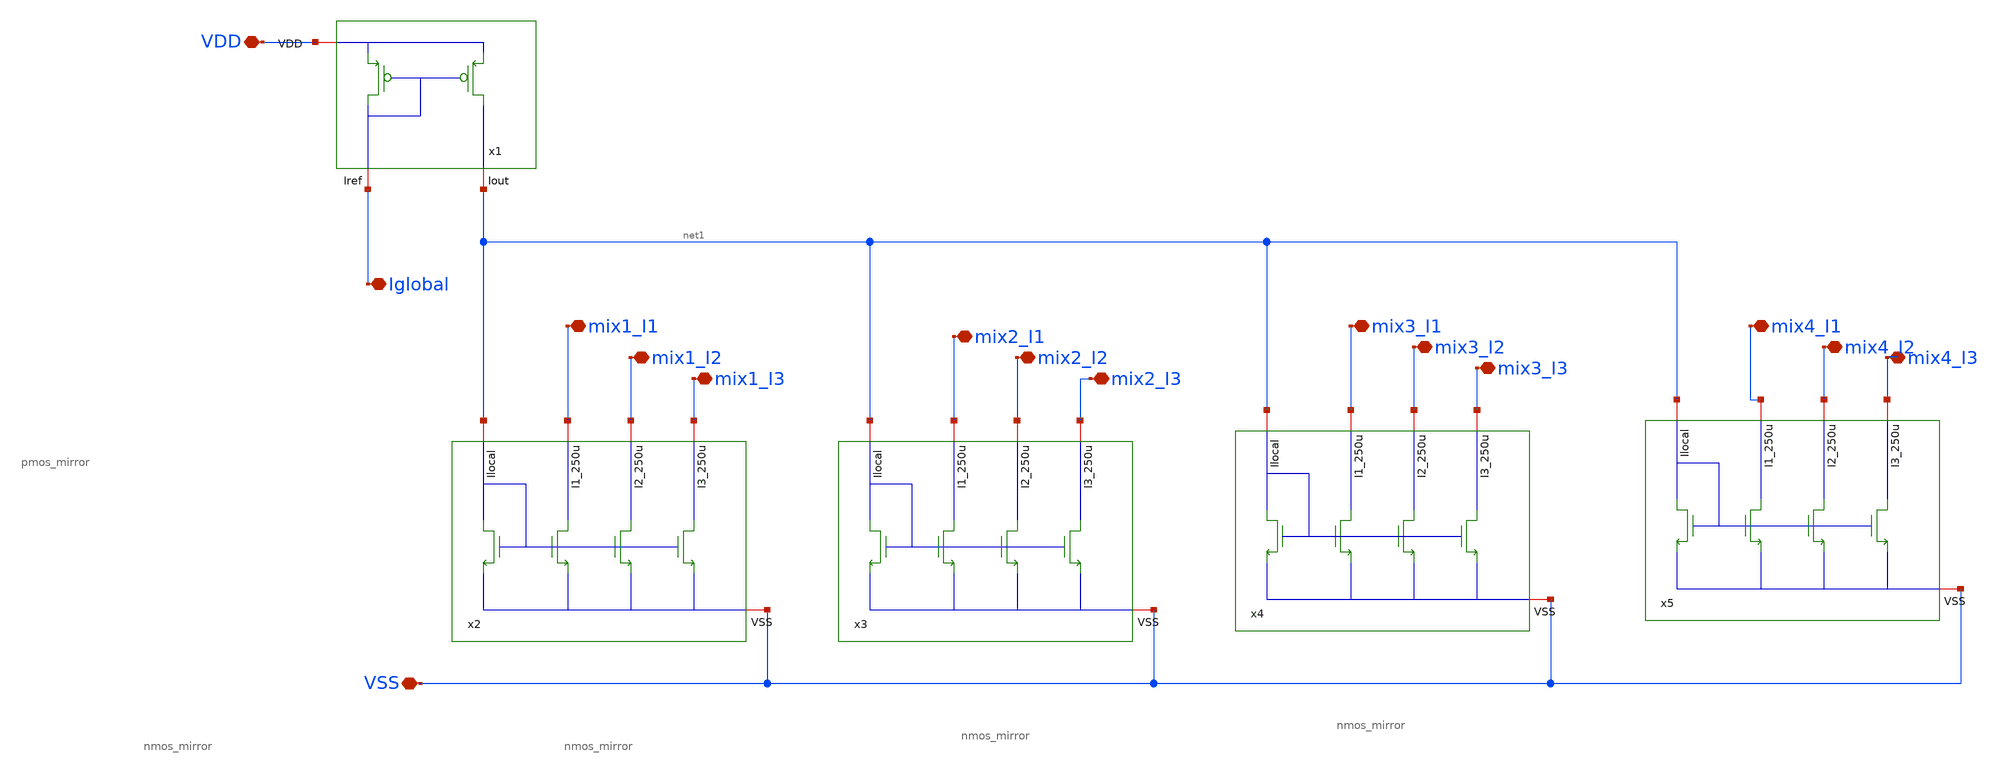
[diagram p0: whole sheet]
** sch_path: designs/mirrors/schematic/mirror_network.sch
**.subckt mirror_network VSS VDD Iglobal mix1_I1 mix1_I2 mix1_I3 mix2_I1 mix2_I2 mix2_I3 mix3_I1
*+ mix3_I2 mix3_I3 mix4_I1 mix4_I2 mix4_I3
*.iopin VSS
*.iopin VDD
*.iopin Iglobal
*.iopin mix1_I1
*.iopin mix1_I2
*.iopin mix1_I3
*.iopin mix2_I1
*.iopin mix2_I2
*.iopin mix2_I3
*.iopin mix3_I1
*.iopin mix3_I2
*.iopin mix3_I3
*.iopin mix4_I1
*.iopin mix4_I2
*.iopin mix4_I3
x1 VDD net1 Iglobal pmos_mirror
x2 net1 mix1_I1 mix1_I2 mix1_I3 VSS nmos_mirror
x3 net1 mix2_I1 mix2_I2 mix2_I3 VSS nmos_mirror
x4 net1 mix3_I1 mix3_I2 mix3_I3 VSS nmos_mirror
x5 net1 mix4_I1 mix4_I2 mix4_I3 VSS nmos_mirror
**.ends
.end
